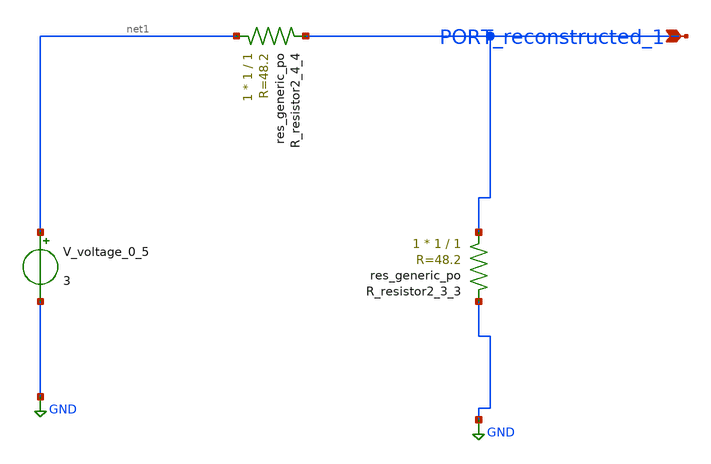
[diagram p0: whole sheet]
** sch_path: schematics/AMSNet/103.sch
**.subckt 103 PORT_reconstructed_1
*.ipin PORT_reconstructed_1
XR_resistor2_3_3 PORT_reconstructed_1 GND sky130_fd_pr__res_generic_po W=1 L=1 m=1
XR_resistor2_4_4 net1 PORT_reconstructed_1 sky130_fd_pr__res_generic_po W=1 L=1 m=1
V_voltage_0_5 net1 GND 3
**.ends
.GLOBAL GND
.end
